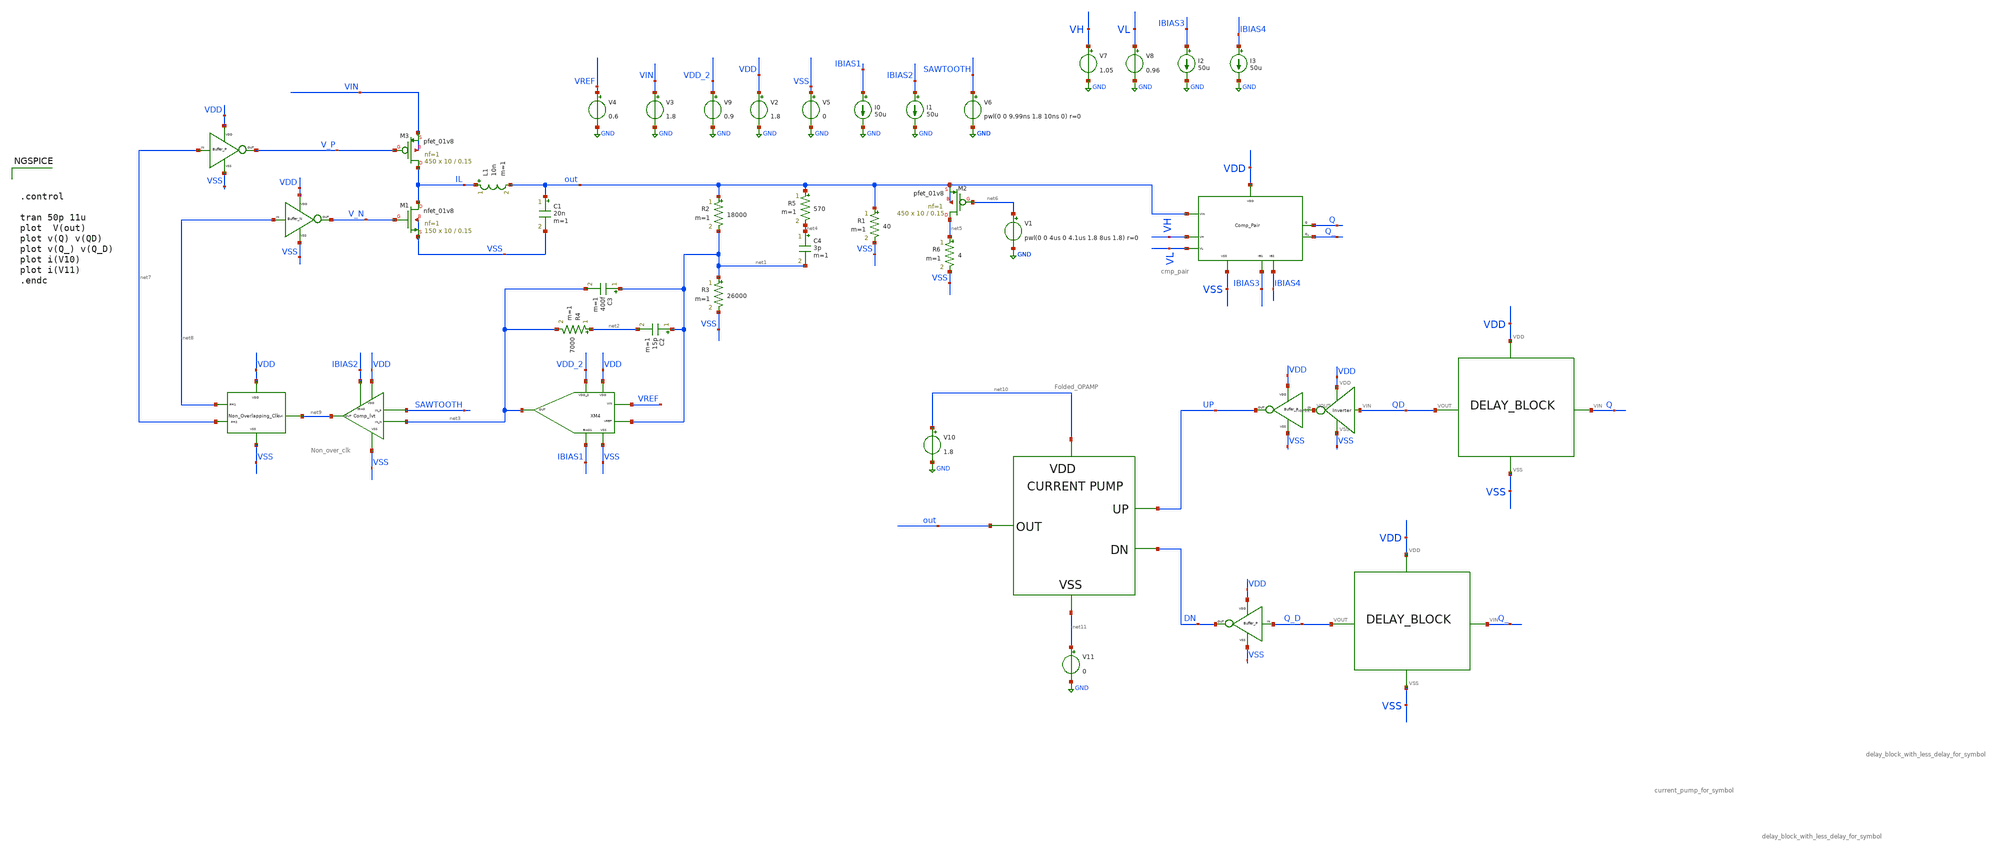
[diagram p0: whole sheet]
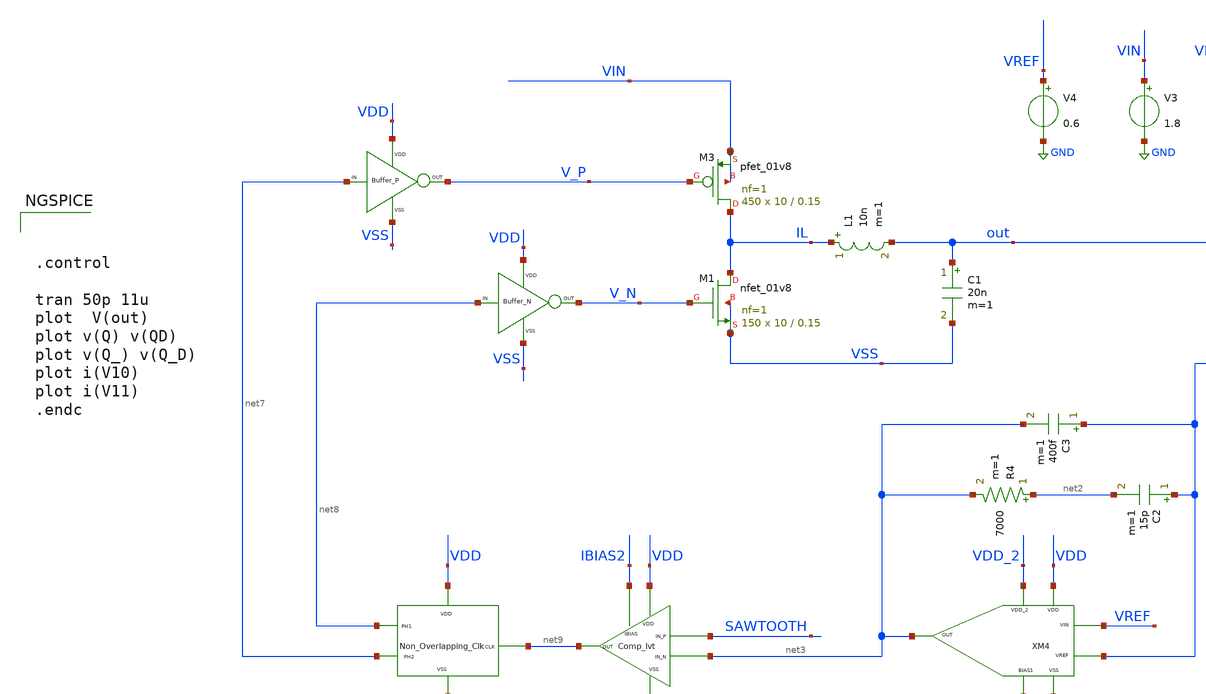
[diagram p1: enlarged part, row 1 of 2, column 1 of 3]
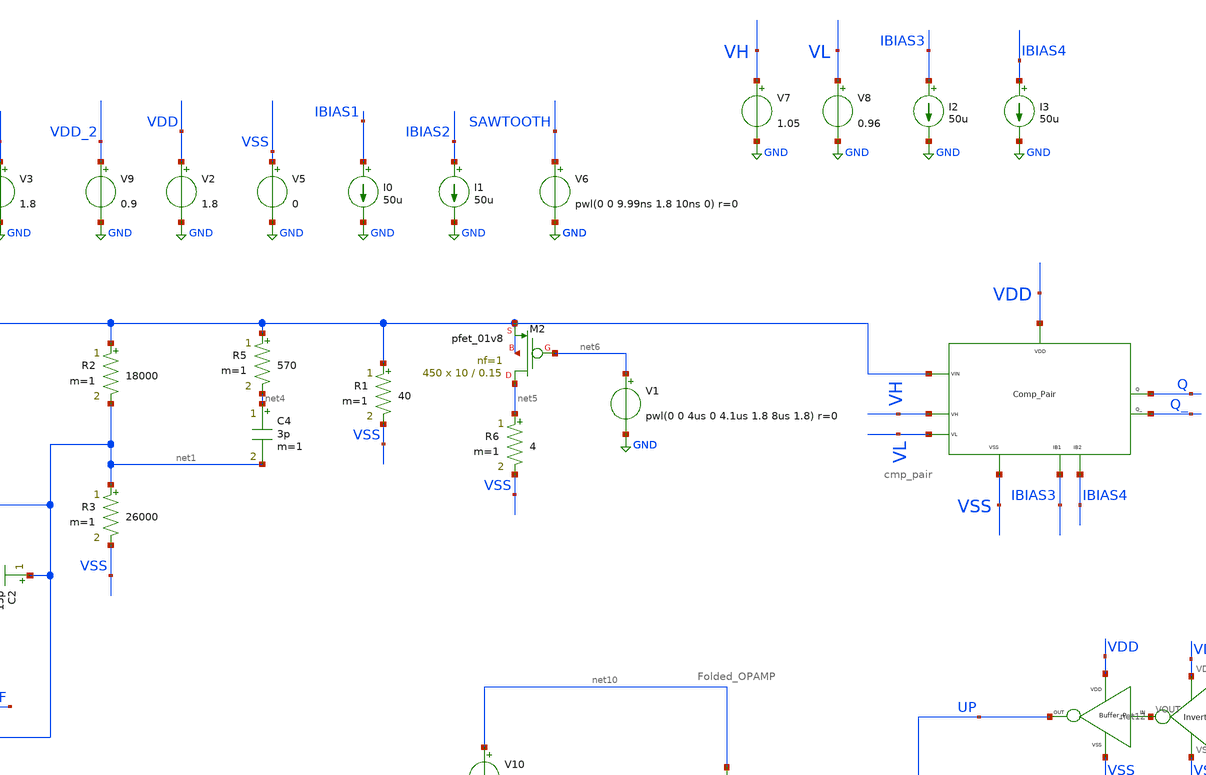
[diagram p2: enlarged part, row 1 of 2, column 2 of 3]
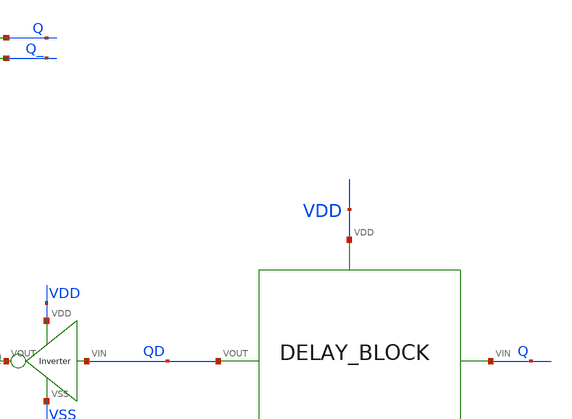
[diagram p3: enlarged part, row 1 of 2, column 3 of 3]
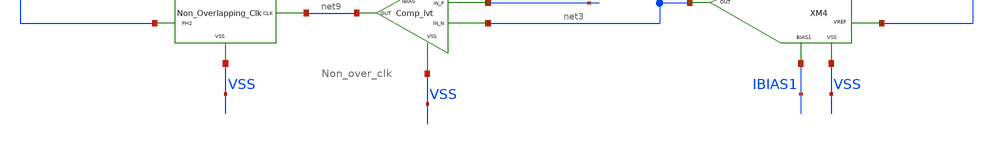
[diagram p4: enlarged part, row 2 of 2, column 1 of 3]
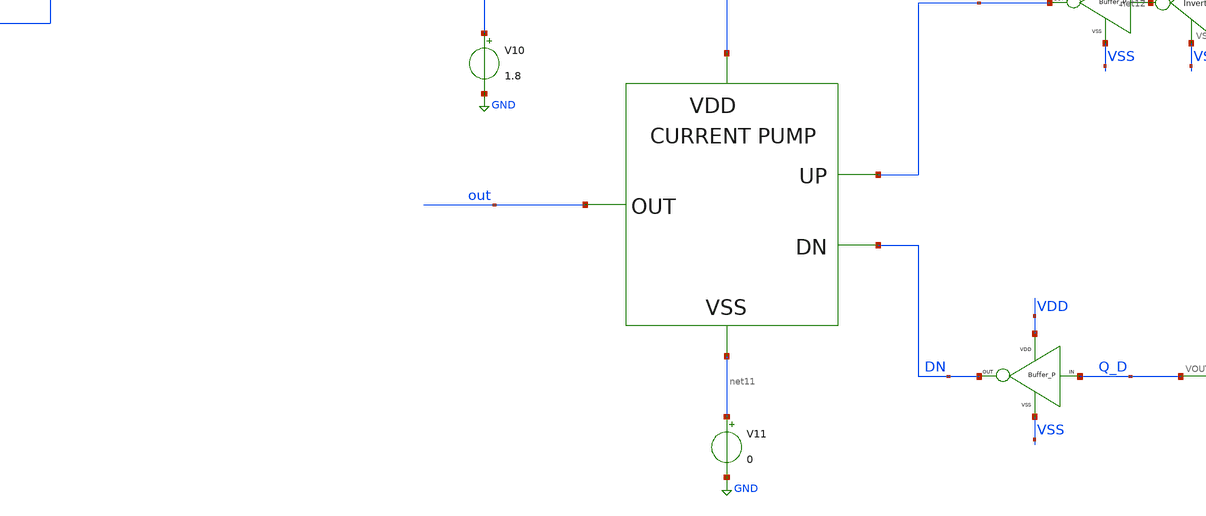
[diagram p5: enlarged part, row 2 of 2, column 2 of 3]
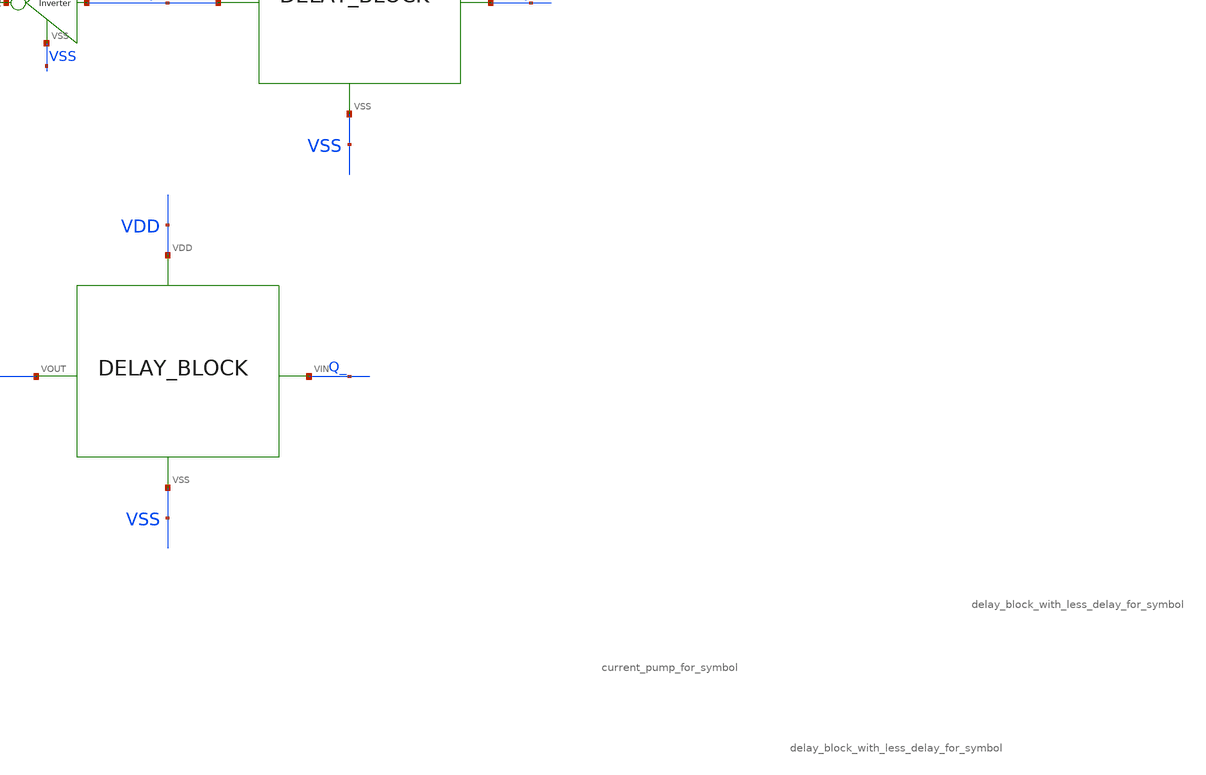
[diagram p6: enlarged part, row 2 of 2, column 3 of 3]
** sch_path: xschem/DC_DC_Converter_xschem/OTHERS/DC_DC_Converter_2/DC_DC_Converter/TOP_LEVEL/closed_loop_v7.sch
**.subckt closed_loop_v7
XM3 IL V_P VIN VIN sky130_fd_pr__pfet_01v8 L=0.15 W=10 nf=1 ad='int((nf+1)/2) * W/nf * 0.29' as='int((nf+2)/2) * W/nf * 0.29'
+ pd='2*int((nf+1)/2) * (W/nf + 0.29)' ps='2*int((nf+2)/2) * (W/nf + 0.29)' nrd='0.29 / W' nrs='0.29 / W'
+ sa=0 sb=0 sd=0 mult=450 m=450
L1 IL out 10n m=1
C1 out VSS 20n m=1
V3 VIN GND 1.8
I0 IBIAS1 GND 50u
V9 VDD_2 GND 0.9
V2 VDD GND 1.8
V5 VSS GND 0
V4 VREF GND 0.6
I1 IBIAS2 GND 50u
V6 SAWTOOTH GND pwl(0 0 9.99ns 1.8 10ns 0) r=0
R2 out net1 18000 m=1
R3 net1 VSS 26000 m=1
R4 net2 net3 7000 m=1
C2 net1 net2 15p m=1
C3 net1 net3 400f m=1
R5 out net4 570 m=1
C4 net4 net1 3p m=1
R1 out VSS 40 m=1
XM1 IL V_N VSS VSS sky130_fd_pr__nfet_01v8 L=0.15 W=10 nf=1 ad='int((nf+1)/2) * W/nf * 0.29' as='int((nf+2)/2) * W/nf * 0.29'
+ pd='2*int((nf+1)/2) * (W/nf + 0.29)' ps='2*int((nf+2)/2) * (W/nf + 0.29)' nrd='0.29 / W' nrs='0.29 / W'
+ sa=0 sb=0 sd=0 mult=150 m=150
XM2 net5 net6 out out sky130_fd_pr__pfet_01v8 L=0.15 W=10 nf=1 ad='int((nf+1)/2) * W/nf * 0.29' as='int((nf+2)/2) * W/nf * 0.29'
+ pd='2*int((nf+1)/2) * (W/nf + 0.29)' ps='2*int((nf+2)/2) * (W/nf + 0.29)' nrd='0.29 / W' nrs='0.29 / W'
+ sa=0 sb=0 sd=0 mult=450 m=450
R6 net5 VSS 4 m=1
V1 net6 GND pwl(0 0 4us 0 4.1us 1.8 8us 1.8) r=0
X1 net7 V_P VDD VSS BUFFER_P
X2 net8 V_N VDD VSS BUFFER_N
XM3 net9 VDD VSS net8 net7 Non_over_clk
XM4 VDD VSS VDD_2 IBIAS1 net3 VREF net1 Folded_OPAMP
XM2 IBIAS2 VDD SAWTOOTH net3 VSS net9 Comp_lvt
V7 VH GND 1.05
V8 VL GND 0.96
I2 IBIAS3 GND 50u
I3 IBIAS4 GND 50u
XM1 VDD VSS out VH VL IBIAS3 IBIAS4 Q Q_ cmp_pair
X3 Q QD VDD VSS delay_block_with_less_delay_for_symbol
X4 Q_ Q_D VDD VSS delay_block_with_less_delay_for_symbol
X5 net12 UP VDD VSS BUFFER_P
X6 Q_D DN VDD VSS BUFFER_P
X7 UP out net10 net11 DN current_pump_for_symbol
V10 net10 GND 1.8
V11 net11 GND 0
X8 VSS VDD QD net12 Inverter
**** begin user architecture code

** opencircuitdesign pdks install
.lib $::SKYWATER_MODELS/sky130.lib.spice tt





.control

tran 50p 11u
plot  V(out)
plot v(Q) v(QD)
plot v(Q_) v(Q_D)
plot i(V10)
plot i(V11)
.endc


**** end user architecture code
**.ends
.GLOBAL GND
.end
